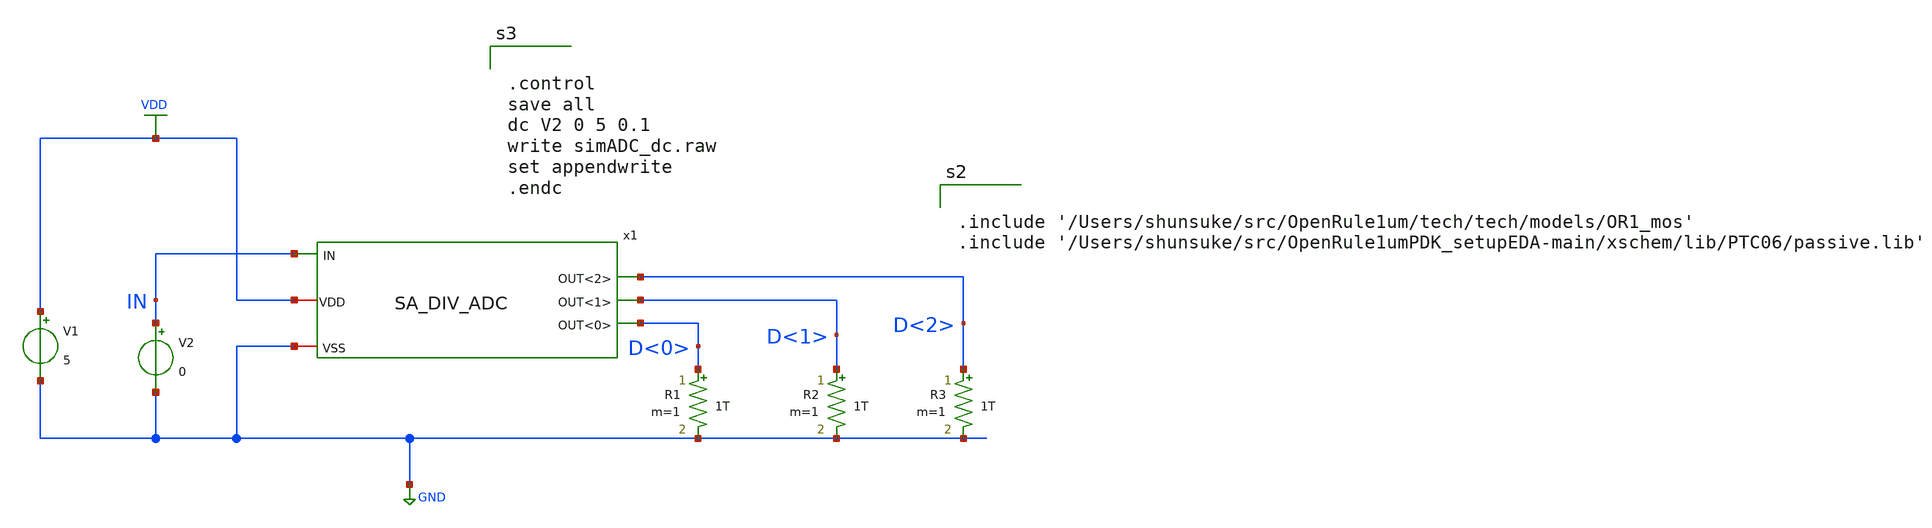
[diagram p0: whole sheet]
** sch_path: design/xschem/testbench/testADC.sch
**.subckt testADC
V1 VDD GND 5
.save i(v1)
x1 VDD IN D<1> D<0> D<2> GND SA_DIV_ADC
R1 D<0> GND 1T m=1
R2 D<1> GND 1T m=1
R3 D<2> GND 1T m=1
V2 IN GND 0
**** begin user architecture code


.include '/Users/shunsuke/src/OpenRule1um/tech/tech/models/OR1_mos'
.include '/Users/shunsuke/src/OpenRule1umPDK_setupEDA-main/xschem/lib/PTC06/passive.lib'




.control
save all
dc V2 0 5 0.1
write simADC_dc.raw
set appendwrite
.endc


**** end user architecture code
**.ends
.GLOBAL VDD
.GLOBAL GND
.end
